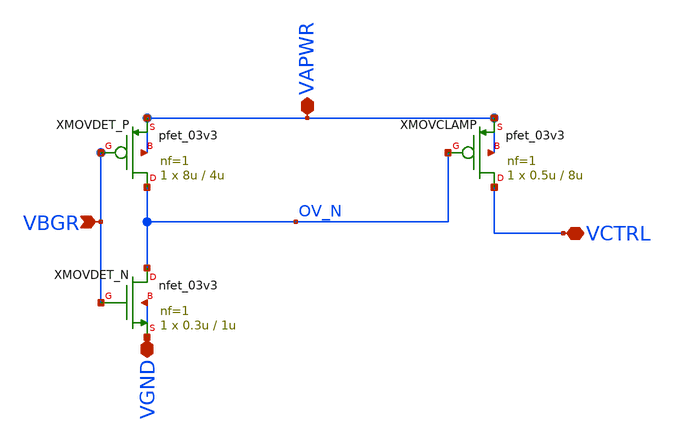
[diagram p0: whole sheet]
** sch_path: xschem/bgr_ov_clamp.sch
**.subckt bgr_ov_clamp VAPWR VGND VBGR VCTRL
*.iopin VAPWR
*.iopin VGND
*.ipin VBGR
*.iopin VCTRL
XMOVDET_N OV_N VBGR VGND VGND nfet_03v3 L=1u W=0.3u nf=1 ad='int((nf+1)/2) * W/nf * 0.18u' as='int((nf+2)/2) * W/nf * 0.18u'
+ pd='2*int((nf+1)/2) * (W/nf + 0.18u)' ps='2*int((nf+2)/2) * (W/nf + 0.18u)' nrd='0.18u / W' nrs='0.18u / W'
+ sa=0 sb=0 sd=0 m=1
XMOVDET_P OV_N VBGR VAPWR VAPWR pfet_03v3 L=4u W=8u nf=1 ad='int((nf+1)/2) * W/nf * 0.18u' as='int((nf+2)/2) * W/nf * 0.18u'
+ pd='2*int((nf+1)/2) * (W/nf + 0.18u)' ps='2*int((nf+2)/2) * (W/nf + 0.18u)' nrd='0.18u / W' nrs='0.18u / W'
+ sa=0 sb=0 sd=0 m=1
XMOVCLAMP VCTRL OV_N VAPWR VAPWR pfet_03v3 L=8u W=0.5u nf=1 ad='int((nf+1)/2) * W/nf * 0.18u' as='int((nf+2)/2) * W/nf * 0.18u'
+ pd='2*int((nf+1)/2) * (W/nf + 0.18u)' ps='2*int((nf+2)/2) * (W/nf + 0.18u)' nrd='0.18u / W' nrs='0.18u / W'
+ sa=0 sb=0 sd=0 m=1
**.ends
.end
